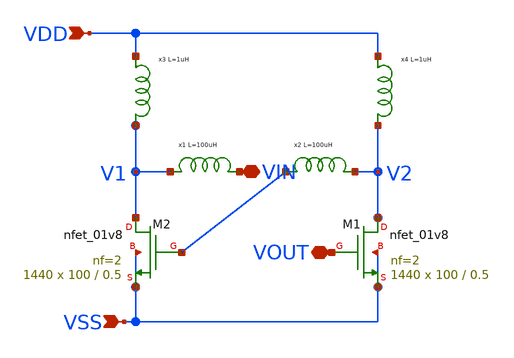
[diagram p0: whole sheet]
** sch_path: design/LELO_SVOD_SKY130A/LELO_EXSC_LOOP.sch
**.subckt LELO_EXSC_LOOP VSS VDD VIN VOUT
*.ipin VSS
*.ipin VDD
*.iopin VIN
*.iopin VOUT
XM1 V2 VOUT VSS VSS sky130_fd_pr__nfet_01v8 L=0.5 W=100 nf=2 ad='int((nf+1)/2) * W/nf * 0.29' as='int((nf+2)/2) * W/nf * 0.29'
+ pd='2*int((nf+1)/2) * (W/nf + 0.29)' ps='2*int((nf+2)/2) * (W/nf + 0.29)' nrd='0.29 / W' nrs='0.29 / W'
+ sa=0 sb=0 sd=0 mult=1440 m=1440
XM2 V1 net1 VSS VSS sky130_fd_pr__nfet_01v8 L=0.5 W=100 nf=2 ad='int((nf+1)/2) * W/nf * 0.29' as='int((nf+2)/2) * W/nf * 0.29'
+ pd='2*int((nf+1)/2) * (W/nf + 0.29)' ps='2*int((nf+2)/2) * (W/nf + 0.29)' nrd='0.29 / W' nrs='0.29 / W'
+ sa=0 sb=0 sd=0 mult=1440 m=1440
x1 V1 VIN MLF2012C101KT000_p
x2 net1 V2 MLF2012C101KT000_p
x3 VDD V1 MLF2012A1R0JT000_p
x4 VDD V2 MLF2012A1R0JT000_p
**.ends

* expanding   symbol:  LELO_SVOD_SKY130A/MLF2012C101KT000_p.sym # of pins=2
** sym_path: design/LELO_SVOD_SKY130A/MLF2012C101KT000_p.sym
.SUBCKT MLF2012C101KT000_p n1 n2
C1 13 17 2.53913456E-12
C2 n1 18 1.59562912E-12
L1 n1 11 1.71914388E-07
L2 11 12 1.82626669E-05
L3 12 13 7.93253796E-05
L4 12 17 4.49576054E-04
L5 13 14 6.53075255E-07
L6 14 15 1.51947035E-06
L7 15 16 4.33477754E-06
R1 11 12 8.80004396E+03
R2 12 13 4.43326588E+04
R3 12 17 9.30797466E+03
R4 n2 13 3.96223318E+01
R5 n2 14 1.93379287E+01
R6 n2 15 9.43799798E+00
R7 n2 16 4.60627439E+00
R8 n2 18 2.00000000E+01
R9 n1 n2 1.00000000E+09
.ENDS MLF2012C101KT000_p

* expanding   symbol:  LELO_SVOD_SKY130A/MLF2012A1R0JT000_p.sym # of pins=2
** sym_path: design/LELO_SVOD_SKY130A/MLF2012A1R0JT000_p.sym
.SUBCKT MLF2012A1R0JT000_p n1 n2
C1 13 17 4.51173927E-12
C2 n1 18 9.42055438E-13
L1 n1 11 1.22046627E-08
L2 11 12 1.81373699E-07
L3 12 13 7.83278932E-07
L4 12 17 3.34324717E-06
L5 13 14 7.78598512E-09
L6 14 15 1.81151766E-08
L7 15 16 5.16793633E-08
R1 11 12 4.74034174E+02
R2 12 13 8.06355781E+05
R3 12 17 6.05296016E+02
R4 n2 13 2.37733991E+00
R5 n2 14 1.16027572E+00
R6 n2 15 5.66279879E-01
R7 n2 16 2.76376463E-01
R8 n2 18 2.00000000E+01
R9 n1 n2 1.00000000E+09
.ENDS MLF2012A1R0JT000_p
.end
